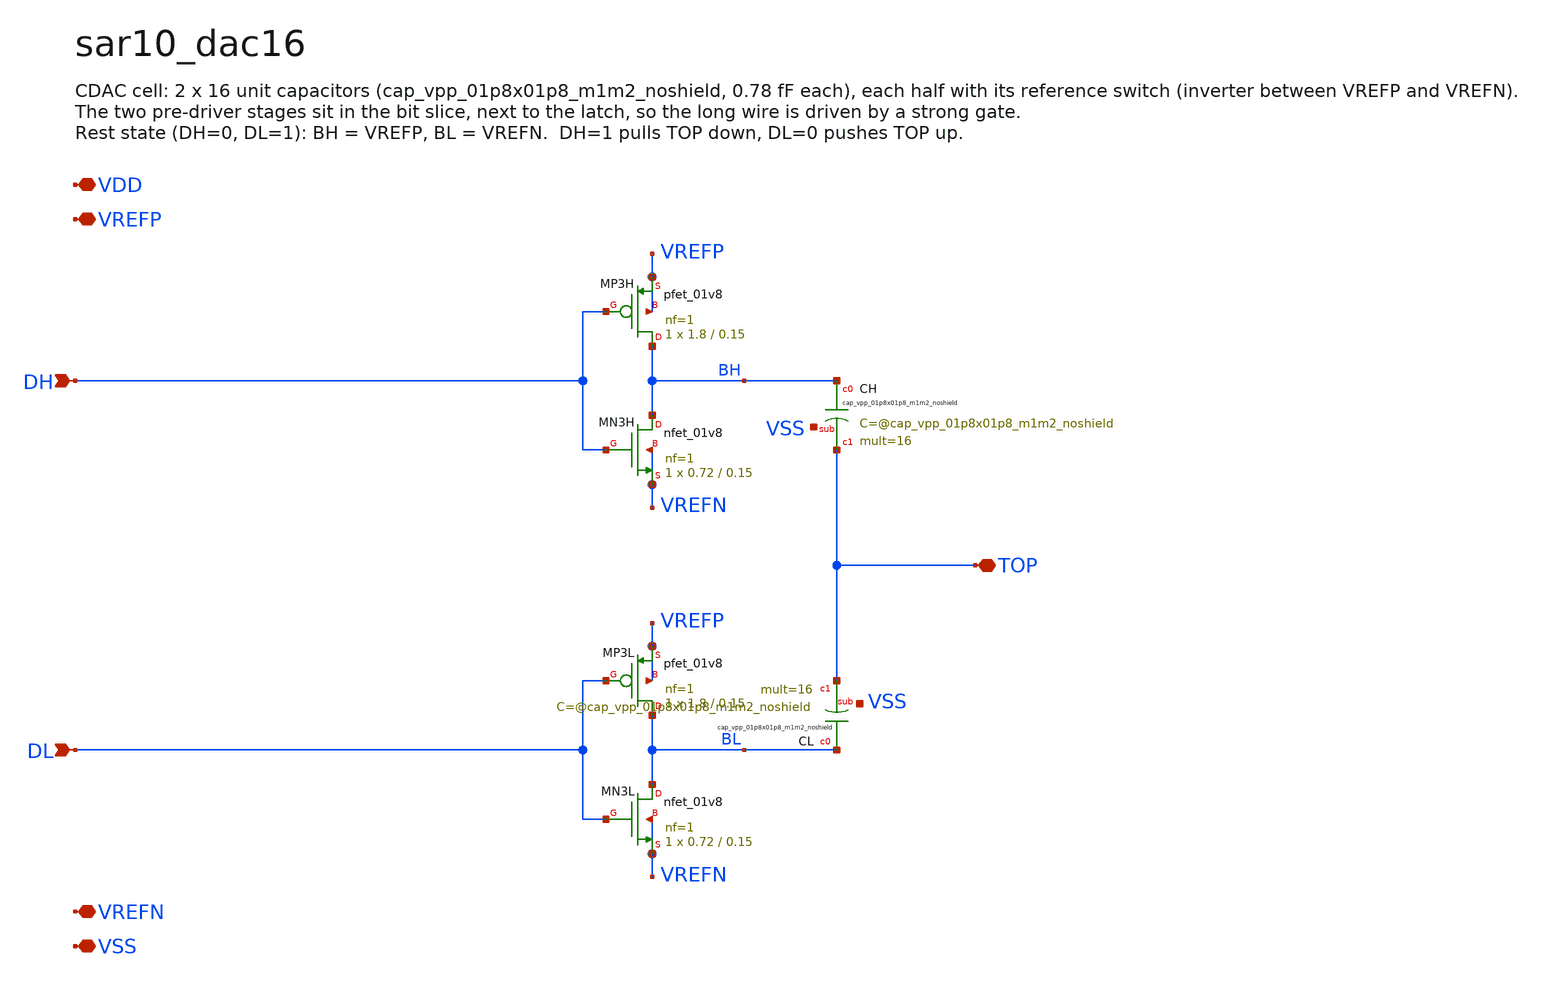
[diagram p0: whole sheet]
** sch_path: xschem/sar10_dac16.sch
**.subckt sar10_dac16 DH DL TOP VDD VREFP VREFN VSS
*.ipin DH
*.ipin DL
*.iopin TOP
*.iopin VDD
*.iopin VREFP
*.iopin VREFN
*.iopin VSS
XMP3H BH DH VREFP VREFP sky130_fd_pr__pfet_01v8 L=0.15 W=1.8 nf=1 ad='int((1 + 1)/2) * 1.8 / 1 * 0.29'
+ as='int((1 + 2)/2) * 1.8 / 1 * 0.29' pd='2*int((1 + 1)/2) * (1.8 / 1 + 0.29)' ps='2*int((1 + 2)/2) * (1.8 / 1 + 0.29)'
+ nrd='0.29 / 1.8 ' nrs='0.29 / 1.8 ' sa=0 sb=0 sd=0 mult=1 m=1
XMN3H BH DH VREFN VREFN sky130_fd_pr__nfet_01v8 L=0.15 W=0.72 nf=1 ad='int((1 + 1)/2) * 0.72 / 1 * 0.29'
+ as='int((1 + 2)/2) * 0.72 / 1 * 0.29' pd='2*int((1 + 1)/2) * (0.72 / 1 + 0.29)' ps='2*int((1 + 2)/2) * (0.72 / 1 + 0.29)'
+ nrd='0.29 / 0.72 ' nrs='0.29 / 0.72 ' sa=0 sb=0 sd=0 mult=1 m=1
XMP3L BL DL VREFP VREFP sky130_fd_pr__pfet_01v8 L=0.15 W=1.8 nf=1 ad='int((1 + 1)/2) * 1.8 / 1 * 0.29'
+ as='int((1 + 2)/2) * 1.8 / 1 * 0.29' pd='2*int((1 + 1)/2) * (1.8 / 1 + 0.29)' ps='2*int((1 + 2)/2) * (1.8 / 1 + 0.29)'
+ nrd='0.29 / 1.8 ' nrs='0.29 / 1.8 ' sa=0 sb=0 sd=0 mult=1 m=1
XMN3L BL DL VREFN VREFN sky130_fd_pr__nfet_01v8 L=0.15 W=0.72 nf=1 ad='int((1 + 1)/2) * 0.72 / 1 * 0.29'
+ as='int((1 + 2)/2) * 0.72 / 1 * 0.29' pd='2*int((1 + 1)/2) * (0.72 / 1 + 0.29)' ps='2*int((1 + 2)/2) * (0.72 / 1 + 0.29)'
+ nrd='0.29 / 0.72 ' nrs='0.29 / 0.72 ' sa=0 sb=0 sd=0 mult=1 m=1
XCH BH TOP VSS sky130_fd_pr__cap_vpp_01p8x01p8_m1m2_noshield mult=16 m=16
XCL BL TOP VSS sky130_fd_pr__cap_vpp_01p8x01p8_m1m2_noshield mult=16 m=16
**.ends
.end
